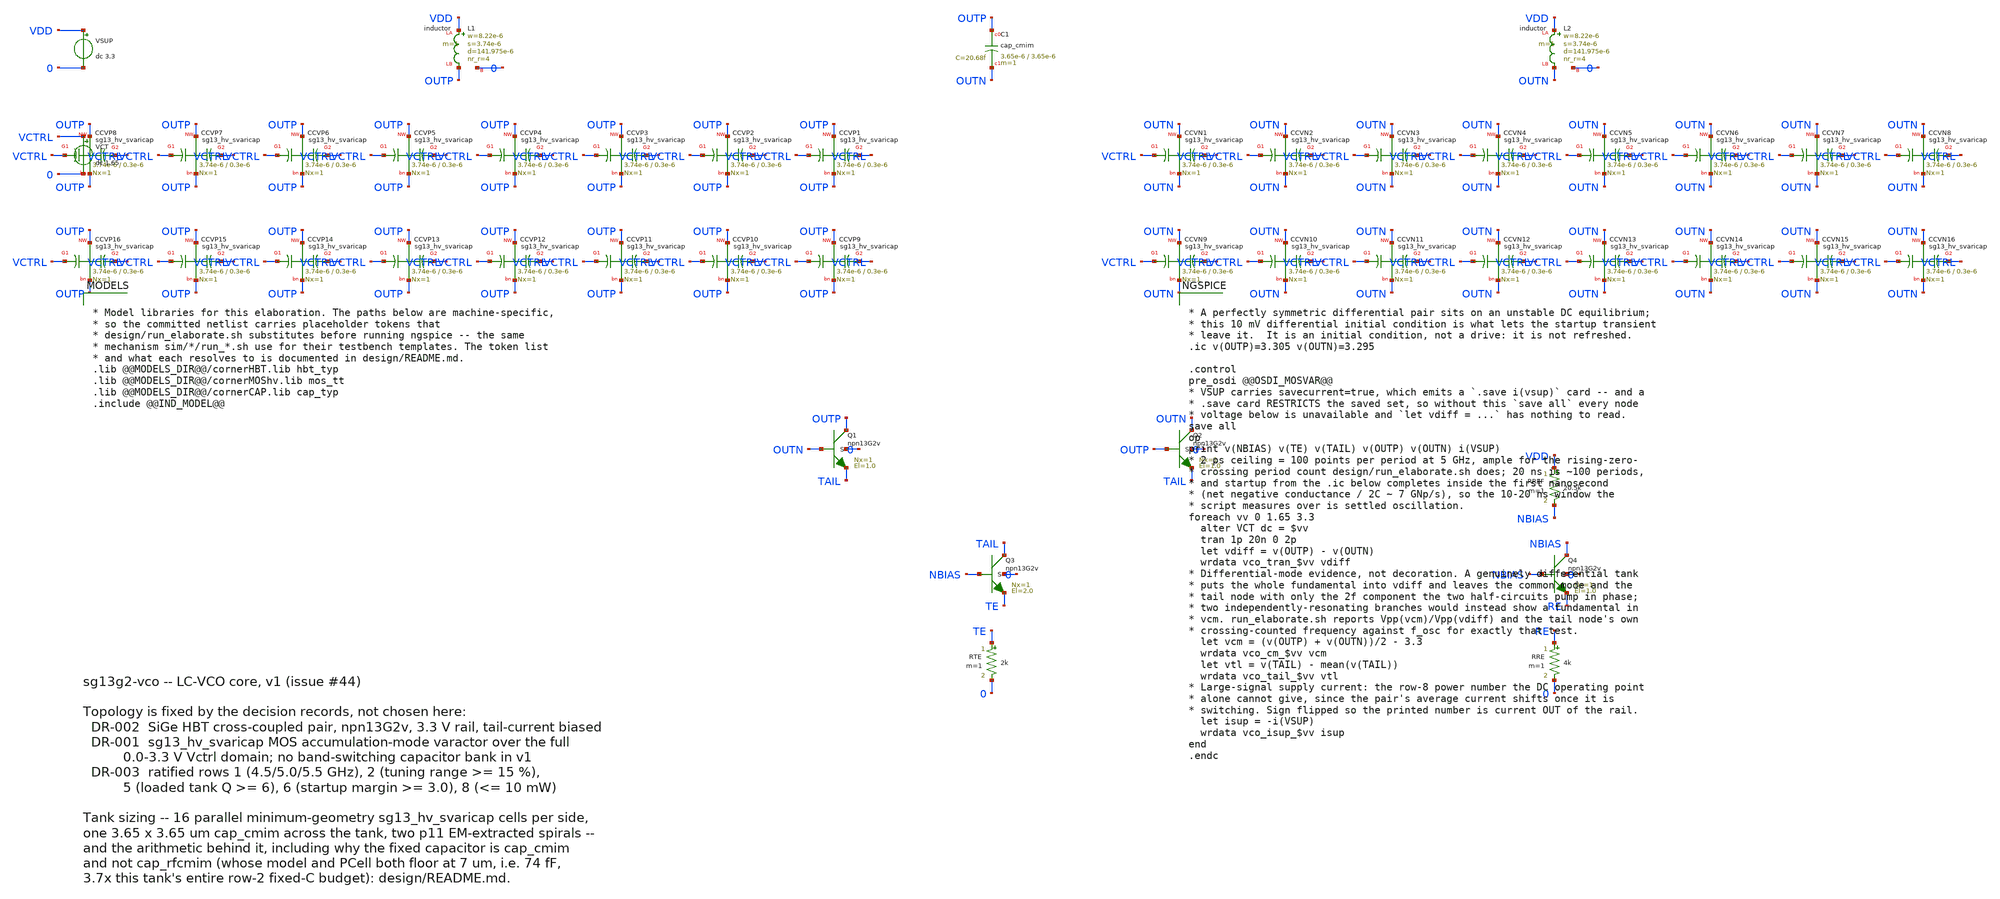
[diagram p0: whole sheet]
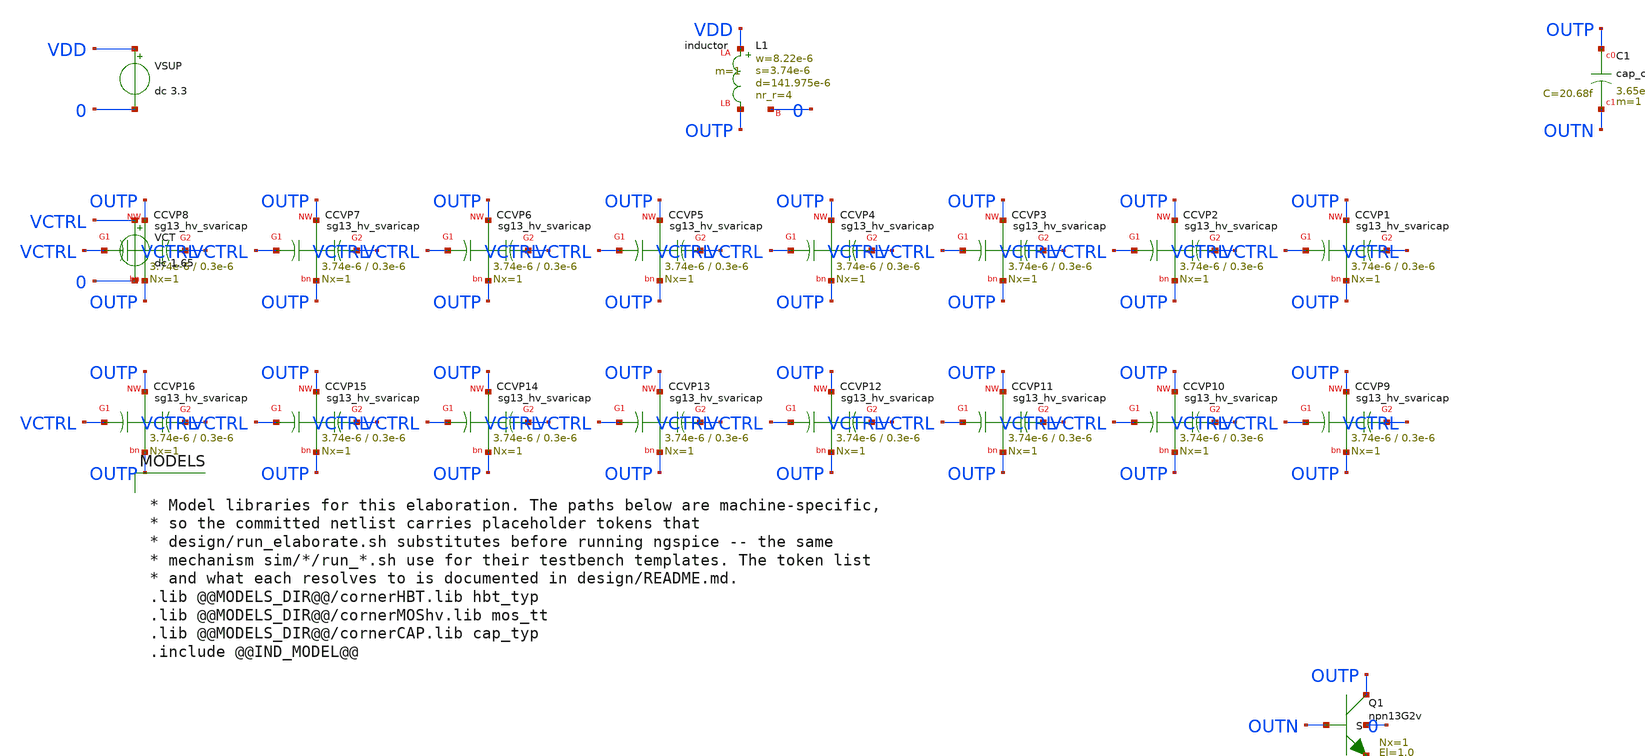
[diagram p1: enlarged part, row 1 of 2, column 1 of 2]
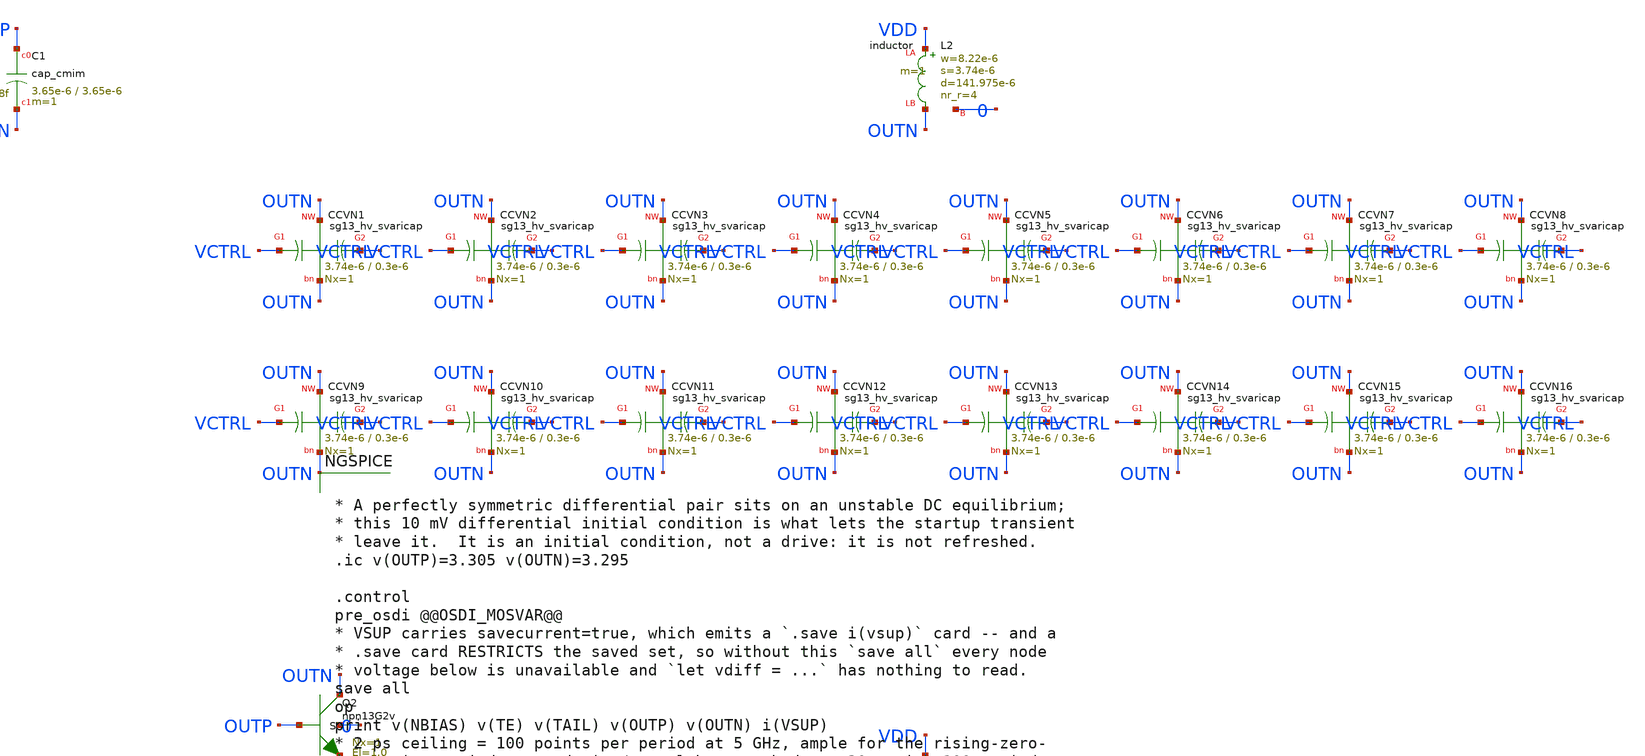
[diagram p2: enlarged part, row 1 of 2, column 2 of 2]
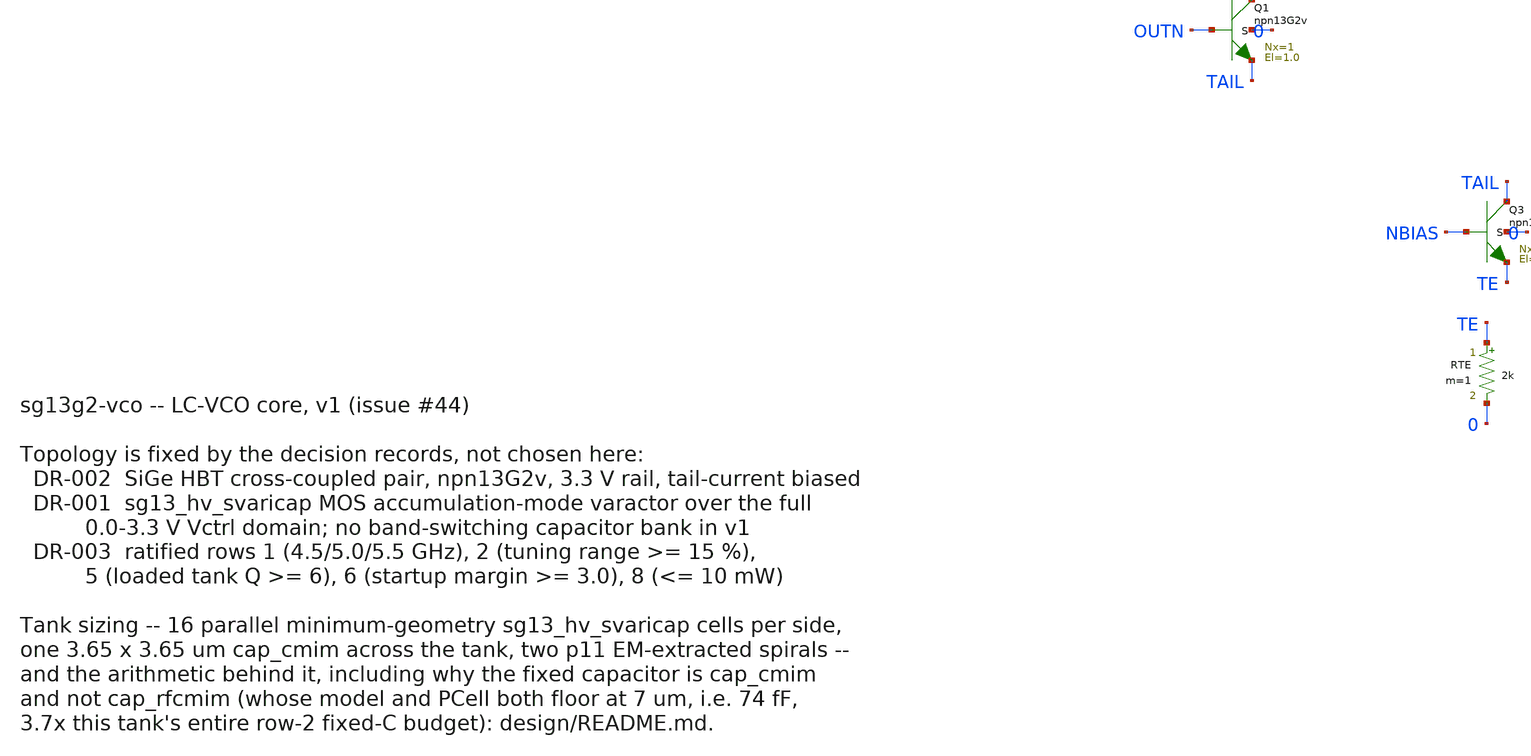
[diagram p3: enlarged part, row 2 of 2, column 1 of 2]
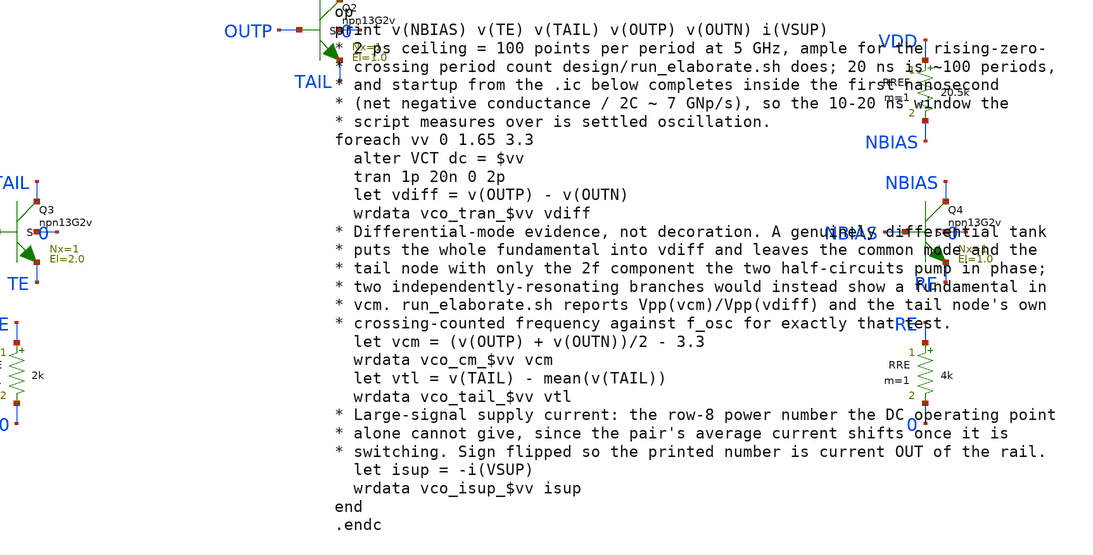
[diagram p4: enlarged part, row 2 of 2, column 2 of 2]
** sch_path: design/vco.sch
**.subckt vco
XL1 VDD OUTP 0 inductor w=8.22e-6 s=3.74e-6 d=141.975e-6 nr_r=4 m=1
XL2 VDD OUTN 0 inductor w=8.22e-6 s=3.74e-6 d=141.975e-6 nr_r=4 m=1
XC1 OUTP OUTN cap_cmim w=3.65e-6 l=3.65e-6 m=1 mm_ok=1
XCVP1 VCTRL OUTP VCTRL OUTP sg13_hv_svaricap w=3.74e-6 l=0.3e-6 Nx=1
XCVP2 VCTRL OUTP VCTRL OUTP sg13_hv_svaricap w=3.74e-6 l=0.3e-6 Nx=1
XCVP3 VCTRL OUTP VCTRL OUTP sg13_hv_svaricap w=3.74e-6 l=0.3e-6 Nx=1
XCVP4 VCTRL OUTP VCTRL OUTP sg13_hv_svaricap w=3.74e-6 l=0.3e-6 Nx=1
XCVP5 VCTRL OUTP VCTRL OUTP sg13_hv_svaricap w=3.74e-6 l=0.3e-6 Nx=1
XCVP6 VCTRL OUTP VCTRL OUTP sg13_hv_svaricap w=3.74e-6 l=0.3e-6 Nx=1
XCVP7 VCTRL OUTP VCTRL OUTP sg13_hv_svaricap w=3.74e-6 l=0.3e-6 Nx=1
XCVP8 VCTRL OUTP VCTRL OUTP sg13_hv_svaricap w=3.74e-6 l=0.3e-6 Nx=1
XCVP9 VCTRL OUTP VCTRL OUTP sg13_hv_svaricap w=3.74e-6 l=0.3e-6 Nx=1
XCVP10 VCTRL OUTP VCTRL OUTP sg13_hv_svaricap w=3.74e-6 l=0.3e-6 Nx=1
XCVP11 VCTRL OUTP VCTRL OUTP sg13_hv_svaricap w=3.74e-6 l=0.3e-6 Nx=1
XCVP12 VCTRL OUTP VCTRL OUTP sg13_hv_svaricap w=3.74e-6 l=0.3e-6 Nx=1
XCVP13 VCTRL OUTP VCTRL OUTP sg13_hv_svaricap w=3.74e-6 l=0.3e-6 Nx=1
XCVP14 VCTRL OUTP VCTRL OUTP sg13_hv_svaricap w=3.74e-6 l=0.3e-6 Nx=1
XCVP15 VCTRL OUTP VCTRL OUTP sg13_hv_svaricap w=3.74e-6 l=0.3e-6 Nx=1
XCVP16 VCTRL OUTP VCTRL OUTP sg13_hv_svaricap w=3.74e-6 l=0.3e-6 Nx=1
XCVN1 VCTRL OUTN VCTRL OUTN sg13_hv_svaricap w=3.74e-6 l=0.3e-6 Nx=1
XCVN2 VCTRL OUTN VCTRL OUTN sg13_hv_svaricap w=3.74e-6 l=0.3e-6 Nx=1
XCVN3 VCTRL OUTN VCTRL OUTN sg13_hv_svaricap w=3.74e-6 l=0.3e-6 Nx=1
XCVN4 VCTRL OUTN VCTRL OUTN sg13_hv_svaricap w=3.74e-6 l=0.3e-6 Nx=1
XCVN5 VCTRL OUTN VCTRL OUTN sg13_hv_svaricap w=3.74e-6 l=0.3e-6 Nx=1
XCVN6 VCTRL OUTN VCTRL OUTN sg13_hv_svaricap w=3.74e-6 l=0.3e-6 Nx=1
XCVN7 VCTRL OUTN VCTRL OUTN sg13_hv_svaricap w=3.74e-6 l=0.3e-6 Nx=1
XCVN8 VCTRL OUTN VCTRL OUTN sg13_hv_svaricap w=3.74e-6 l=0.3e-6 Nx=1
XCVN9 VCTRL OUTN VCTRL OUTN sg13_hv_svaricap w=3.74e-6 l=0.3e-6 Nx=1
XCVN10 VCTRL OUTN VCTRL OUTN sg13_hv_svaricap w=3.74e-6 l=0.3e-6 Nx=1
XCVN11 VCTRL OUTN VCTRL OUTN sg13_hv_svaricap w=3.74e-6 l=0.3e-6 Nx=1
XCVN12 VCTRL OUTN VCTRL OUTN sg13_hv_svaricap w=3.74e-6 l=0.3e-6 Nx=1
XCVN13 VCTRL OUTN VCTRL OUTN sg13_hv_svaricap w=3.74e-6 l=0.3e-6 Nx=1
XCVN14 VCTRL OUTN VCTRL OUTN sg13_hv_svaricap w=3.74e-6 l=0.3e-6 Nx=1
XCVN15 VCTRL OUTN VCTRL OUTN sg13_hv_svaricap w=3.74e-6 l=0.3e-6 Nx=1
XCVN16 VCTRL OUTN VCTRL OUTN sg13_hv_svaricap w=3.74e-6 l=0.3e-6 Nx=1
XQ1 OUTP OUTN TAIL 0 npn13G2v Nx=1 El=1.0 mm_ok=1
XQ2 OUTN OUTP TAIL 0 npn13G2v Nx=1 El=1.0 mm_ok=1
XQ3 TAIL NBIAS TE 0 npn13G2v Nx=1 El=2.0 mm_ok=1
RTE TE 0 2k m=1
RREF VDD NBIAS 20.5k m=1
XQ4 NBIAS NBIAS RE 0 npn13G2v Nx=1 El=1.0 mm_ok=1
RRE RE 0 4k m=1
VSUP VDD 0 dc 3.3
.save i(vsup)
VCT VCTRL 0 dc 1.65
**** begin user architecture code


* Model libraries for this elaboration. The paths below are machine-specific,
* so the committed netlist carries placeholder tokens that
* design/run_elaborate.sh substitutes before running ngspice -- the same
* mechanism sim/*/run_*.sh use for their testbench templates. The token list
* and what each resolves to is documented in design/README.md.
.lib @@MODELS_DIR@@/cornerHBT.lib hbt_typ
.lib @@MODELS_DIR@@/cornerMOShv.lib mos_tt
.lib @@MODELS_DIR@@/cornerCAP.lib cap_typ
.include @@IND_MODEL@@




* A perfectly symmetric differential pair sits on an unstable DC equilibrium;
* this 10 mV differential initial condition is what lets the startup transient
* leave it.  It is an initial condition, not a drive: it is not refreshed.
.ic v(OUTP)=3.305 v(OUTN)=3.295

.control
pre_osdi @@OSDI_MOSVAR@@
* VSUP carries savecurrent=true, which emits a `.save i(vsup)` card -- and a
* .save card RESTRICTS the saved set, so without this `save all` every node
* voltage below is unavailable and `let vdiff = ...` has nothing to read.
save all
op
print v(NBIAS) v(TE) v(TAIL) v(OUTP) v(OUTN) i(VSUP)
* 2 ps ceiling = 100 points per period at 5 GHz, ample for the rising-zero-
* crossing period count design/run_elaborate.sh does; 20 ns is ~100 periods,
* and startup from the .ic below completes inside the first nanosecond
* (net negative conductance / 2C ~ 7 GNp/s), so the 10-20 ns window the
* script measures over is settled oscillation.
foreach vv 0 1.65 3.3
  alter VCT dc = $vv
  tran 1p 20n 0 2p
  let vdiff = v(OUTP) - v(OUTN)
  wrdata vco_tran_$vv vdiff
* Differential-mode evidence, not decoration. A genuinely differential tank
* puts the whole fundamental into vdiff and leaves the common mode and the
* tail node with only the 2f component the two half-circuits pump in phase;
* two independently-resonating branches would instead show a fundamental in
* vcm. run_elaborate.sh reports Vpp(vcm)/Vpp(vdiff) and the tail node's own
* crossing-counted frequency against f_osc for exactly that test.
  let vcm = (v(OUTP) + v(OUTN))/2 - 3.3
  wrdata vco_cm_$vv vcm
  let vtl = v(TAIL) - mean(v(TAIL))
  wrdata vco_tail_$vv vtl
* Large-signal supply current: the row-8 power number the DC operating point
* alone cannot give, since the pair's average current shifts once it is
* switching. Sign flipped so the printed number is current OUT of the rail.
  let isup = -i(VSUP)
  wrdata vco_isup_$vv isup
end
.endc


**** end user architecture code
**.ends
.end
